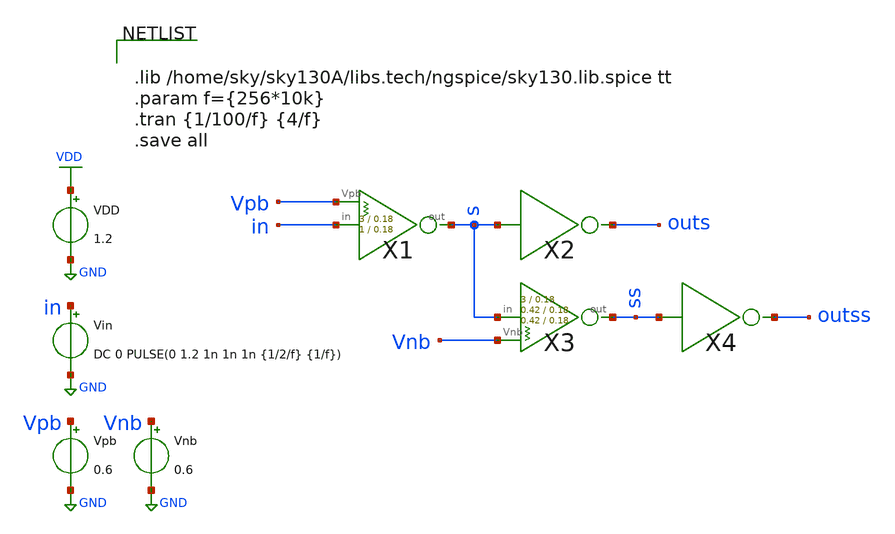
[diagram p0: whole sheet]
** sch_path: xschem/inv/inv_weak_pullup_pulldown_tb.sch
**.subckt inv_weak_pullup_pulldown_tb
Vin in GND DC 0 PULSE(0 1.2 1n 1n 1n {1/2/f} {1/f})
VDD VDD GND 1.2
X1 in s Vpb inv_weak_pullup Wpmos=3 Lpmos=0.18 Wnmos=1 Lnmos=0.18
Vpb Vpb GND 0.6
X2 s outs inv
Vnb Vnb GND 0.6
X3 s ss Vnb inv_weak_pulldown Wpmos=3 Lpmos=0.18 Wnmos=1 Lnmos=0.18
X4 ss outss inv
**** begin user architecture code


.lib /home/sky/sky130A/libs.tech/ngspice/sky130.lib.spice tt
.param f={256*10k}
.tran {1/100/f} {4/f}
.save all


**** end user architecture code
**.ends
.GLOBAL VDD
.GLOBAL GND
.end
